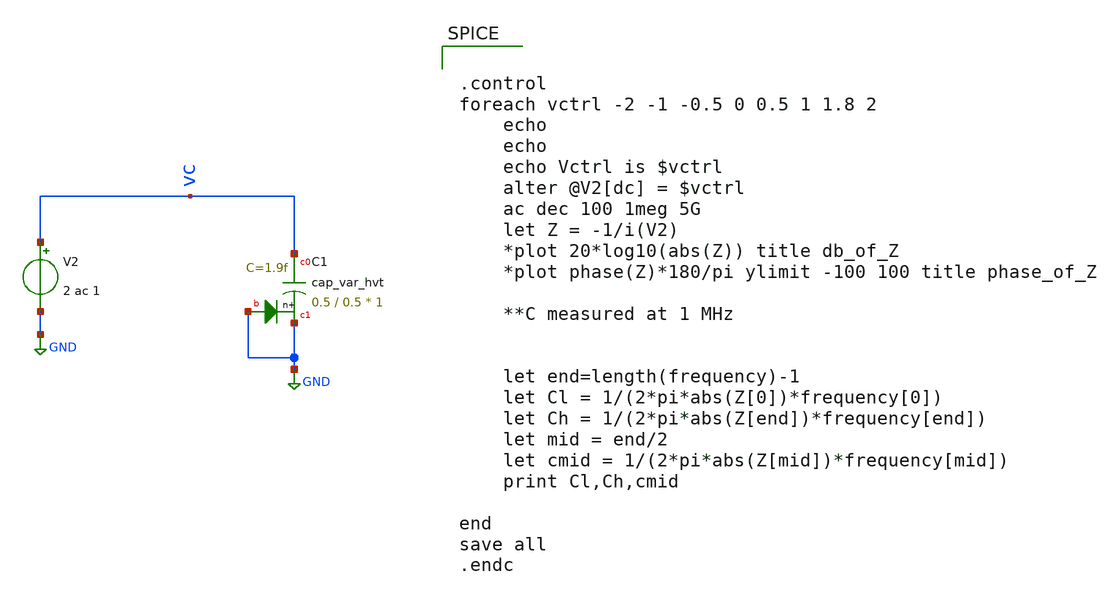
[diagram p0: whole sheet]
** sch_path: varactor_meas/hvtvarchar.sch
**.subckt hvtvarchar
V2 vc GND 2 ac 1
XC1 vc GND GND sky130_fd_pr__cap_var_hvt W=0.5 L=0.5 VM=1 m=1
**** begin user architecture code


.control
foreach vctrl -2 -1 -0.5 0 0.5 1 1.8 2
	echo
	echo
	echo Vctrl is $vctrl
	alter @V2[dc] = $vctrl
	ac dec 100 1meg 5G
	let Z = -1/i(V2)
	*plot 20*log10(abs(Z)) title db_of_Z
	*plot phase(Z)*180/pi ylimit -100 100 title phase_of_Z

	**C measured at 1 MHz


	let end=length(frequency)-1
	let Cl = 1/(2*pi*abs(Z[0])*frequency[0])
	let Ch = 1/(2*pi*abs(Z[end])*frequency[end])
	let mid = end/2
	let cmid = 1/(2*pi*abs(Z[mid])*frequency[mid])
	print Cl,Ch,cmid

end
save all
.endc




.option wnflag = 1
.lib /usr/local/share/pdk/sky130A/libs.tech/ngspice/sky130.lib.spice tt
.lib /usr/local/share/pdk/sky130A/libs.ref/spice
.include /usr/local/share/pdk/sky130A/libs.ref/sky130_fd_pr/spice/sky130_fd_pr__ind_05_220.model.spice
.param mc_mm_switch=0


**** end user architecture code
**.ends
.GLOBAL GND
.end
